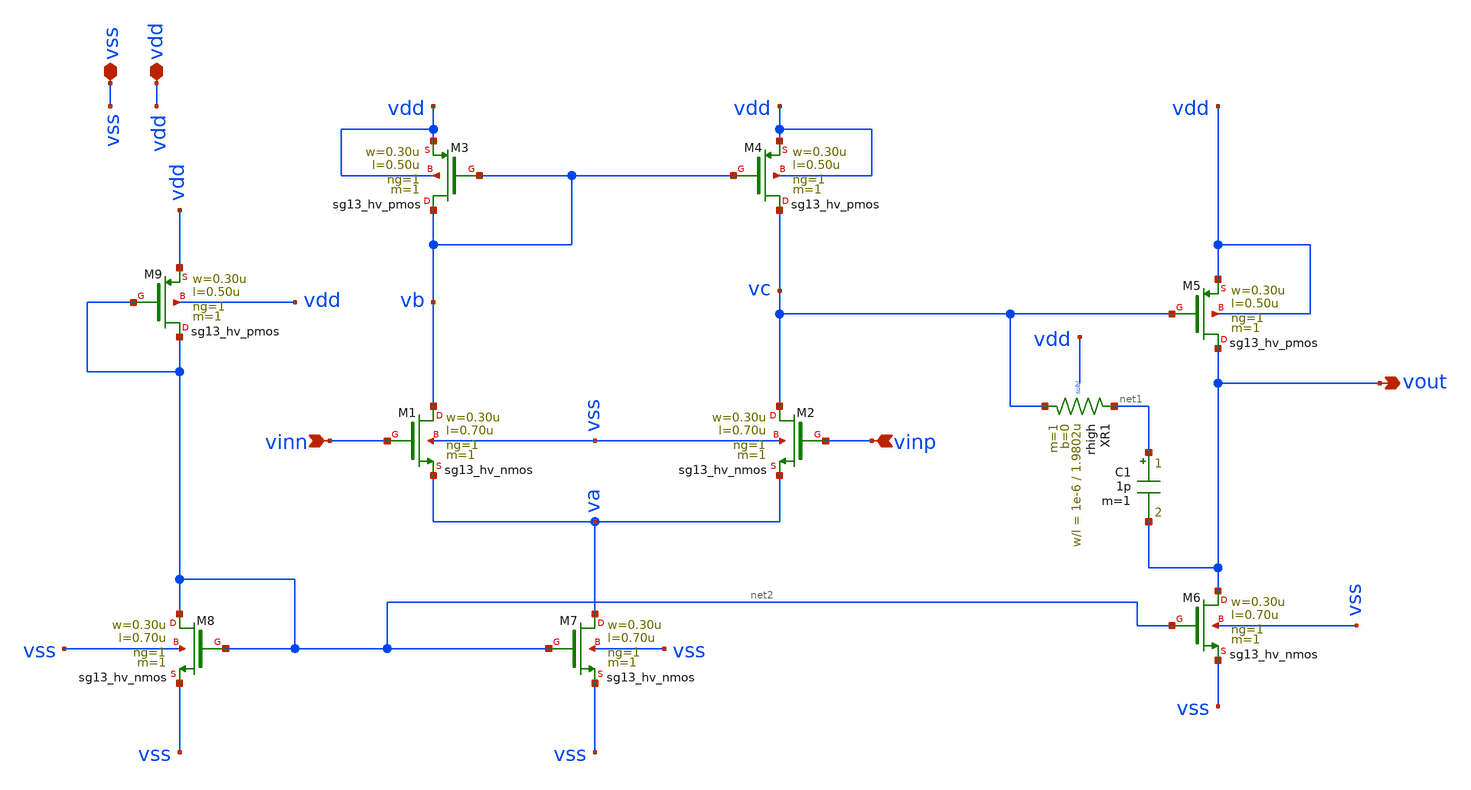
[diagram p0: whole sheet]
** sch_path: analog-db/drawings/ldo-005-ti-ldo-buffer-ref/ihp130/ref_amp/ref_amp_real_current_source.sch
**.subckt ref_amp_real_current_source vinn vinp vdd vss vout
*.ipin vinn
*.ipin vinp
*.iopin vdd
*.iopin vss
*.opin vout
XM1 vb vinn va vss sg13_hv_nmos w=0.30u l=0.70u ng=1 m=1 mm_ok=1
XM2 vc vinp va vss sg13_hv_nmos w=0.30u l=0.70u ng=1 m=1 mm_ok=1
XM3 vb vb vdd vdd sg13_hv_pmos w=0.30u l=0.50u ng=1 m=1 mm_ok=1
XM4 vc vb vdd vdd sg13_hv_pmos w=0.30u l=0.50u ng=1 m=1 mm_ok=1
XM5 vout vc vdd vdd sg13_hv_pmos w=0.30u l=0.50u ng=1 m=1 mm_ok=1
C1 net1 vout 1p m=1
XR1 vc net1 sub! rhigh w=1e-6 l=1.9802u m=1 b=0
XM6 vout net2 vss vss sg13_hv_nmos w=0.30u l=0.70u ng=1 m=1 mm_ok=1
XM7 va net2 vss vss sg13_hv_nmos w=0.30u l=0.70u ng=1 m=1 mm_ok=1
XM8 net2 net2 vss vss sg13_hv_nmos w=0.30u l=0.70u ng=1 m=1 mm_ok=1
XM9 net2 net2 vdd vdd sg13_hv_pmos w=0.30u l=0.50u ng=1 m=1 mm_ok=1
**.ends
.end
